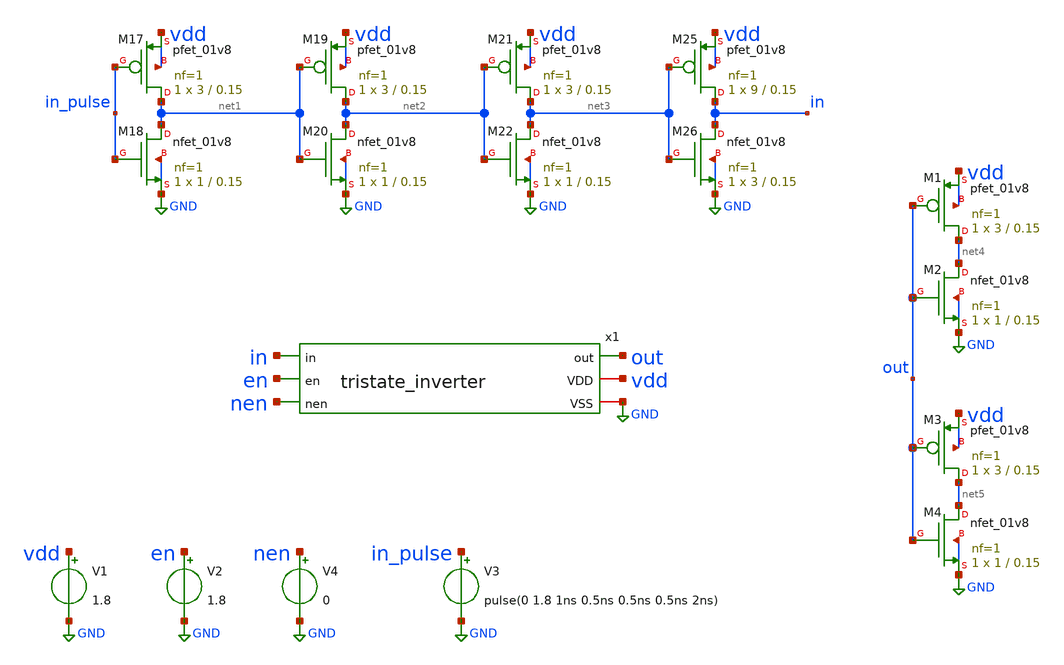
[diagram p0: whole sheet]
** sch_path: xschem/tristate_inverter_tb.sch
**.subckt tristate_inverter_tb
x1 in en nen out vdd GND tristate_inverter
XM17 net1 in_pulse vdd vdd sky130_fd_pr__pfet_01v8 L=0.15 W=3 nf=1 ad='int((nf+1)/2) * W/nf * 0.29' as='int((nf+2)/2) * W/nf * 0.29'
+ pd='2*int((nf+1)/2) * (W/nf + 0.29)' ps='2*int((nf+2)/2) * (W/nf + 0.29)' nrd='0.29 / W' nrs='0.29 / W'
+ sa=0 sb=0 sd=0 mult=1 m=1
XM18 net1 in_pulse GND GND sky130_fd_pr__nfet_01v8 L=0.15 W=1 nf=1 ad='int((nf+1)/2) * W/nf * 0.29' as='int((nf+2)/2) * W/nf * 0.29'
+ pd='2*int((nf+1)/2) * (W/nf + 0.29)' ps='2*int((nf+2)/2) * (W/nf + 0.29)' nrd='0.29 / W' nrs='0.29 / W'
+ sa=0 sb=0 sd=0 mult=1 m=1
XM19 net2 net1 vdd vdd sky130_fd_pr__pfet_01v8 L=0.15 W=3 nf=1 ad='int((nf+1)/2) * W/nf * 0.29' as='int((nf+2)/2) * W/nf * 0.29'
+ pd='2*int((nf+1)/2) * (W/nf + 0.29)' ps='2*int((nf+2)/2) * (W/nf + 0.29)' nrd='0.29 / W' nrs='0.29 / W'
+ sa=0 sb=0 sd=0 mult=1 m=1
XM20 net2 net1 GND GND sky130_fd_pr__nfet_01v8 L=0.15 W=1 nf=1 ad='int((nf+1)/2) * W/nf * 0.29' as='int((nf+2)/2) * W/nf * 0.29'
+ pd='2*int((nf+1)/2) * (W/nf + 0.29)' ps='2*int((nf+2)/2) * (W/nf + 0.29)' nrd='0.29 / W' nrs='0.29 / W'
+ sa=0 sb=0 sd=0 mult=1 m=1
XM21 net3 net2 vdd vdd sky130_fd_pr__pfet_01v8 L=0.15 W=3 nf=1 ad='int((nf+1)/2) * W/nf * 0.29' as='int((nf+2)/2) * W/nf * 0.29'
+ pd='2*int((nf+1)/2) * (W/nf + 0.29)' ps='2*int((nf+2)/2) * (W/nf + 0.29)' nrd='0.29 / W' nrs='0.29 / W'
+ sa=0 sb=0 sd=0 mult=1 m=1
XM22 net3 net2 GND GND sky130_fd_pr__nfet_01v8 L=0.15 W=1 nf=1 ad='int((nf+1)/2) * W/nf * 0.29' as='int((nf+2)/2) * W/nf * 0.29'
+ pd='2*int((nf+1)/2) * (W/nf + 0.29)' ps='2*int((nf+2)/2) * (W/nf + 0.29)' nrd='0.29 / W' nrs='0.29 / W'
+ sa=0 sb=0 sd=0 mult=1 m=1
XM25 in net3 vdd vdd sky130_fd_pr__pfet_01v8 L=0.15 W=9 nf=1 ad='int((nf+1)/2) * W/nf * 0.29' as='int((nf+2)/2) * W/nf * 0.29'
+ pd='2*int((nf+1)/2) * (W/nf + 0.29)' ps='2*int((nf+2)/2) * (W/nf + 0.29)' nrd='0.29 / W' nrs='0.29 / W'
+ sa=0 sb=0 sd=0 mult=1 m=1
XM26 in net3 GND GND sky130_fd_pr__nfet_01v8 L=0.15 W=3 nf=1 ad='int((nf+1)/2) * W/nf * 0.29' as='int((nf+2)/2) * W/nf * 0.29'
+ pd='2*int((nf+1)/2) * (W/nf + 0.29)' ps='2*int((nf+2)/2) * (W/nf + 0.29)' nrd='0.29 / W' nrs='0.29 / W'
+ sa=0 sb=0 sd=0 mult=1 m=1
V1 vdd GND 1.8
V3 in_pulse GND pulse(0 1.8 1ns 0.5ns 0.5ns 0.5ns 2ns)
V2 en GND 1.8
V4 nen GND 0
XM1 net4 out vdd vdd sky130_fd_pr__pfet_01v8 L=0.15 W=3 nf=1 ad='int((nf+1)/2) * W/nf * 0.29' as='int((nf+2)/2) * W/nf * 0.29'
+ pd='2*int((nf+1)/2) * (W/nf + 0.29)' ps='2*int((nf+2)/2) * (W/nf + 0.29)' nrd='0.29 / W' nrs='0.29 / W'
+ sa=0 sb=0 sd=0 mult=1 m=1
XM2 net4 out GND GND sky130_fd_pr__nfet_01v8 L=0.15 W=1 nf=1 ad='int((nf+1)/2) * W/nf * 0.29' as='int((nf+2)/2) * W/nf * 0.29'
+ pd='2*int((nf+1)/2) * (W/nf + 0.29)' ps='2*int((nf+2)/2) * (W/nf + 0.29)' nrd='0.29 / W' nrs='0.29 / W'
+ sa=0 sb=0 sd=0 mult=1 m=1
XM3 net5 out vdd vdd sky130_fd_pr__pfet_01v8 L=0.15 W=3 nf=1 ad='int((nf+1)/2) * W/nf * 0.29' as='int((nf+2)/2) * W/nf * 0.29'
+ pd='2*int((nf+1)/2) * (W/nf + 0.29)' ps='2*int((nf+2)/2) * (W/nf + 0.29)' nrd='0.29 / W' nrs='0.29 / W'
+ sa=0 sb=0 sd=0 mult=1 m=1
XM4 net5 out GND GND sky130_fd_pr__nfet_01v8 L=0.15 W=1 nf=1 ad='int((nf+1)/2) * W/nf * 0.29' as='int((nf+2)/2) * W/nf * 0.29'
+ pd='2*int((nf+1)/2) * (W/nf + 0.29)' ps='2*int((nf+2)/2) * (W/nf + 0.29)' nrd='0.29 / W' nrs='0.29 / W'
+ sa=0 sb=0 sd=0 mult=1 m=1
**** begin user architecture code

** opencircuitdesign pdks install
.lib $::SKYWATER_MODELS/sky130.lib.spice tt





.tran 0.0001n 5n
.save v(in) v(out)

.control
run
set wr_vecnames
wrdata tristate_inverter_9313_tb.txt v(in) v(out)
.endc


**** end user architecture code
**.ends

* expanding   symbol:  tristate_inverter.sym # of pins=6
** sym_path: xschem/tristate_inverter.sym
** sch_path: xschem/tristate_inverter.sch
.subckt tristate_inverter in en nen out VDD VSS
*.iopin VDD
*.ipin in
*.opin out
*.iopin VSS
*.ipin en
*.ipin nen
XM5 out in net2 VDD sky130_fd_pr__pfet_01v8 L=0.15 W=3 nf=1 ad='int((nf+1)/2) * W/nf * 0.29' as='int((nf+2)/2) * W/nf * 0.29'
+ pd='2*int((nf+1)/2) * (W/nf + 0.29)' ps='2*int((nf+2)/2) * (W/nf + 0.29)' nrd='0.29 / W' nrs='0.29 / W'
+ sa=0 sb=0 sd=0 mult=1 m=1
XM7 out in net1 VSS sky130_fd_pr__nfet_01v8 L=0.15 W=1 nf=1 ad='int((nf+1)/2) * W/nf * 0.29' as='int((nf+2)/2) * W/nf * 0.29'
+ pd='2*int((nf+1)/2) * (W/nf + 0.29)' ps='2*int((nf+2)/2) * (W/nf + 0.29)' nrd='0.29 / W' nrs='0.29 / W'
+ sa=0 sb=0 sd=0 mult=1 m=1
XM1 net2 nen VDD VDD sky130_fd_pr__pfet_01v8 L=0.15 W=9 nf=1 ad='int((nf+1)/2) * W/nf * 0.29' as='int((nf+2)/2) * W/nf * 0.29'
+ pd='2*int((nf+1)/2) * (W/nf + 0.29)' ps='2*int((nf+2)/2) * (W/nf + 0.29)' nrd='0.29 / W' nrs='0.29 / W'
+ sa=0 sb=0 sd=0 mult=1 m=1
XM2 net1 en VSS VSS sky130_fd_pr__nfet_01v8 L=0.15 W=3 nf=1 ad='int((nf+1)/2) * W/nf * 0.29' as='int((nf+2)/2) * W/nf * 0.29'
+ pd='2*int((nf+1)/2) * (W/nf + 0.29)' ps='2*int((nf+2)/2) * (W/nf + 0.29)' nrd='0.29 / W' nrs='0.29 / W'
+ sa=0 sb=0 sd=0 mult=1 m=1
.ends

.GLOBAL GND
.end
